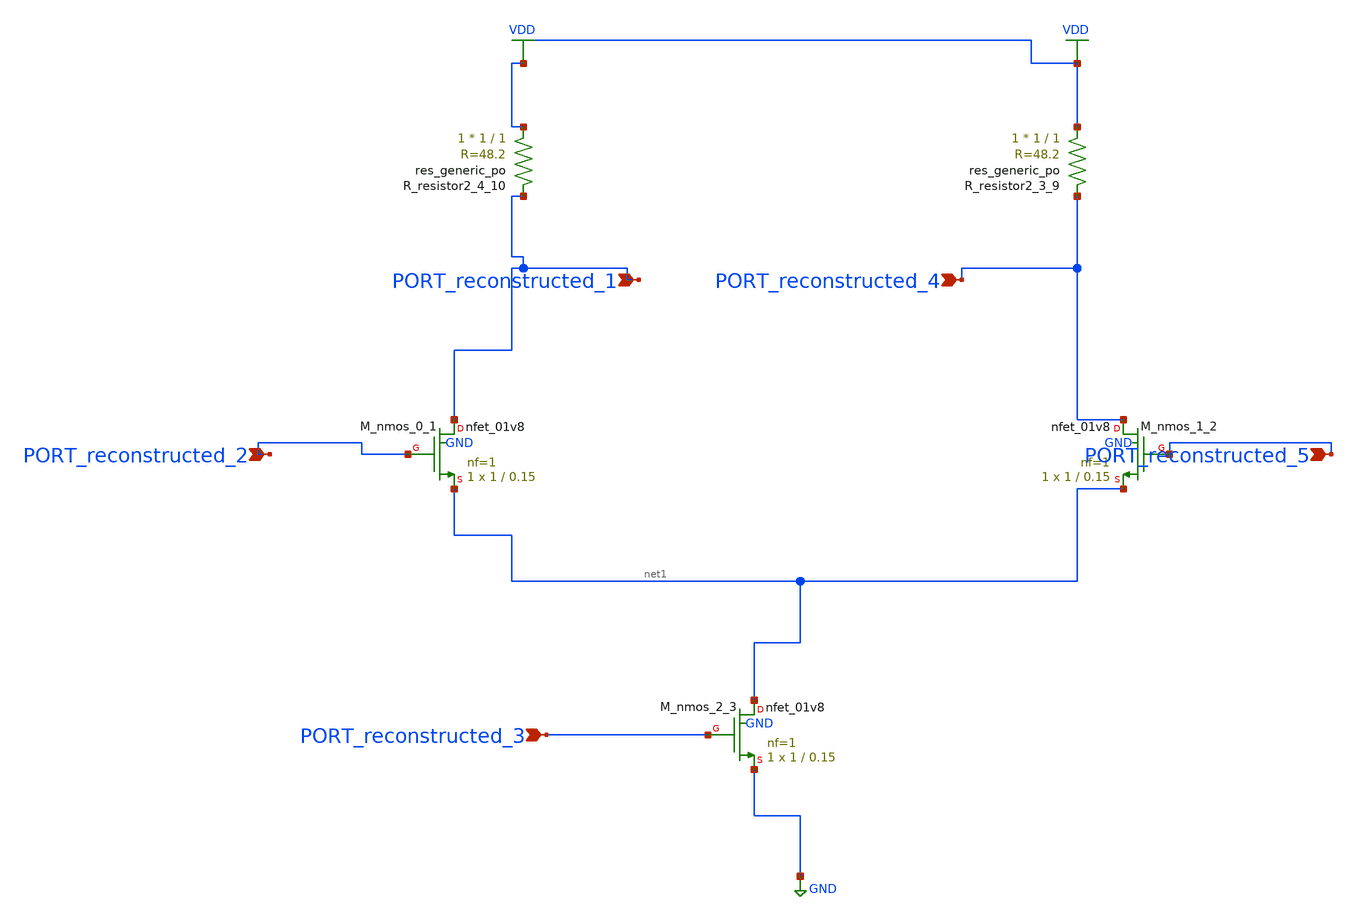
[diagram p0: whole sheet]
** sch_path: schematics/AMSNet/384.sch
**.subckt 384 PORT_reconstructed_2 PORT_reconstructed_3 PORT_reconstructed_4 PORT_reconstructed_5
*+ PORT_reconstructed_1
*.ipin PORT_reconstructed_2
*.ipin PORT_reconstructed_3
*.ipin PORT_reconstructed_4
*.ipin PORT_reconstructed_5
*.ipin PORT_reconstructed_1
XM_nmos_0_1 PORT_reconstructed_1 PORT_reconstructed_2 net1 GND sky130_fd_pr__nfet_01v8 L=0.15 W=1 nf=1
+ ad='int((1 + 1)/2) * 1 / 1 * 0.29' as='int((1 + 2)/2) * 1 / 1 * 0.29' pd='2*int((1 + 1)/2) * (1 / 1 + 0.29)'
+ ps='2*int((1 + 2)/2) * (1 / 1 + 0.29)' nrd='0.29 / 1 ' nrs='0.29 / 1 ' sa=0 sb=0 sd=0 mult=1 m=1
XM_nmos_1_2 PORT_reconstructed_4 PORT_reconstructed_5 net1 GND sky130_fd_pr__nfet_01v8 L=0.15 W=1 nf=1
+ ad='int((1 + 1)/2) * 1 / 1 * 0.29' as='int((1 + 2)/2) * 1 / 1 * 0.29' pd='2*int((1 + 1)/2) * (1 / 1 + 0.29)'
+ ps='2*int((1 + 2)/2) * (1 / 1 + 0.29)' nrd='0.29 / 1 ' nrs='0.29 / 1 ' sa=0 sb=0 sd=0 mult=1 m=1
XM_nmos_2_3 net1 PORT_reconstructed_3 GND GND sky130_fd_pr__nfet_01v8 L=0.15 W=1 nf=1 ad='int((1 + 1)/2) * 1 / 1 * 0.29'
+ as='int((1 + 2)/2) * 1 / 1 * 0.29' pd='2*int((1 + 1)/2) * (1 / 1 + 0.29)' ps='2*int((1 + 2)/2) * (1 / 1 + 0.29)'
+ nrd='0.29 / 1 ' nrs='0.29 / 1 ' sa=0 sb=0 sd=0 mult=1 m=1
XR_resistor2_3_9 VDD PORT_reconstructed_4 sky130_fd_pr__res_generic_po W=1 L=1 m=1
XR_resistor2_4_10 VDD PORT_reconstructed_1 sky130_fd_pr__res_generic_po W=1 L=1 m=1
**.ends
.GLOBAL GND
.GLOBAL VDD
.end
